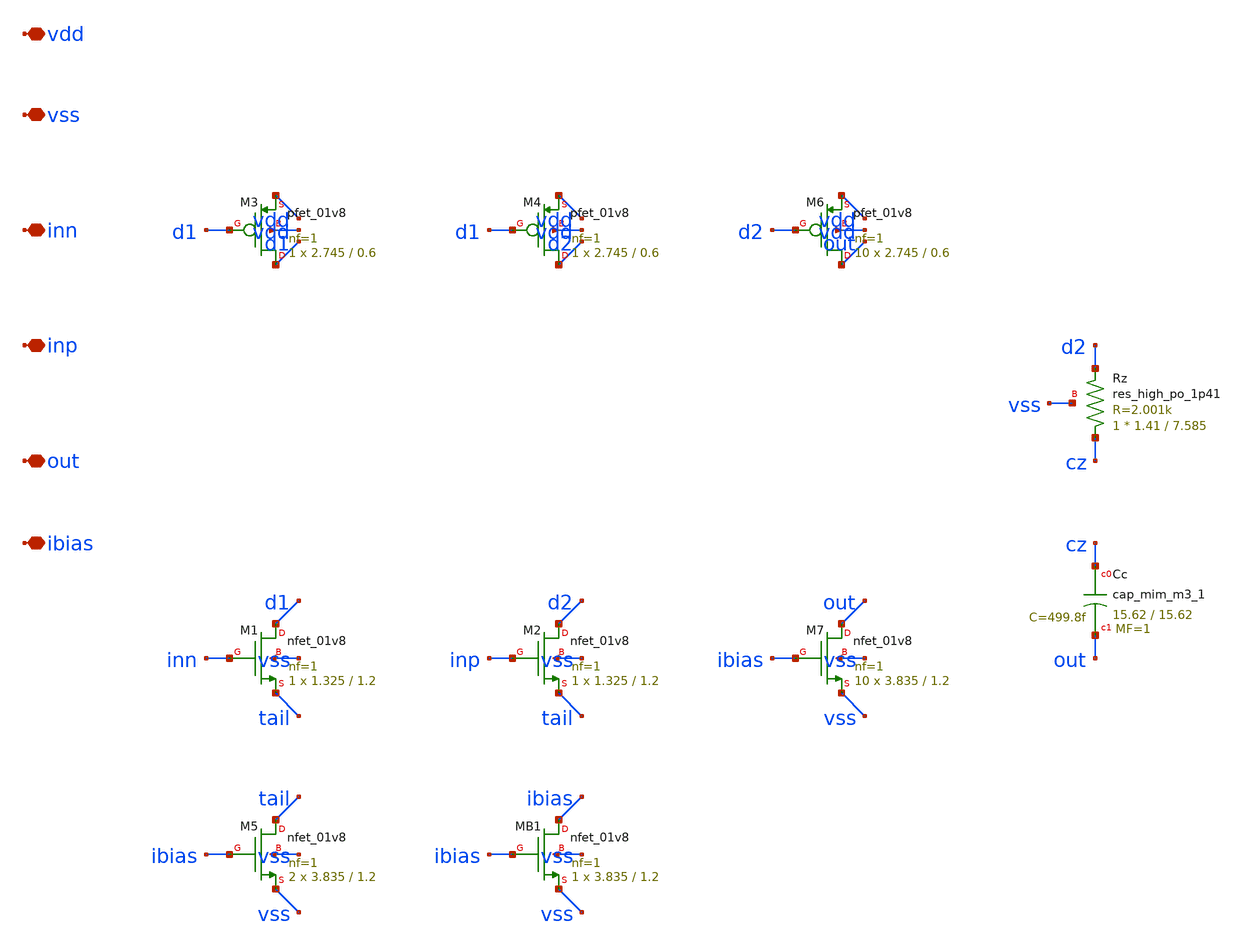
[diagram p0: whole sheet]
** sch_path: design/opamp_core.sch
**.subckt opamp_core vdd vss inn inp out ibias
*.iopin vdd
*.iopin vss
*.iopin inn
*.iopin inp
*.iopin out
*.iopin ibias
XM3 d1 d1 vdd vdd sky130_fd_pr__pfet_01v8 L=0.6 W=2.745 nf=1 ad='int((nf+1)/2) * W/nf * 0.29' as='int((nf+2)/2) * W/nf * 0.29'
+ pd='2*int((nf+1)/2) * (W/nf + 0.29)' ps='2*int((nf+2)/2) * (W/nf + 0.29)' nrd='0.29 / W' nrs='0.29 / W'
+ sa=0 sb=0 sd=0 mult=1 m=1
XM4 d2 d1 vdd vdd sky130_fd_pr__pfet_01v8 L=0.6 W=2.745 nf=1 ad='int((nf+1)/2) * W/nf * 0.29' as='int((nf+2)/2) * W/nf * 0.29'
+ pd='2*int((nf+1)/2) * (W/nf + 0.29)' ps='2*int((nf+2)/2) * (W/nf + 0.29)' nrd='0.29 / W' nrs='0.29 / W'
+ sa=0 sb=0 sd=0 mult=1 m=1
XM1 d1 inn tail vss sky130_fd_pr__nfet_01v8 L=1.2 W=1.325 nf=1 ad='int((1 + 1)/2) * 1.325 / 1 * 0.29'
+ as='int((1 + 2)/2) * 1.325 / 1 * 0.29' pd='2*int((1 + 1)/2) * (1.325 / 1 + 0.29)' ps='2*int((1 + 2)/2) * (1.325 / 1 + 0.29)'
+ nrd='0.29 / 1.325 ' nrs='0.29 / 1.325 ' sa=0 sb=0 sd=0 mult=1 m=1
XM2 d2 inp tail vss sky130_fd_pr__nfet_01v8 L=1.2 W=1.325 nf=1 ad='int((1 + 1)/2) * 1.325 / 1 * 0.29'
+ as='int((1 + 2)/2) * 1.325 / 1 * 0.29' pd='2*int((1 + 1)/2) * (1.325 / 1 + 0.29)' ps='2*int((1 + 2)/2) * (1.325 / 1 + 0.29)'
+ nrd='0.29 / 1.325 ' nrs='0.29 / 1.325 ' sa=0 sb=0 sd=0 mult=1 m=1
XM5 tail ibias vss vss sky130_fd_pr__nfet_01v8 L=1.2 W=3.835 nf=1 ad='int((1 + 1)/2) * 3.835 / 1 * 0.29'
+ as='int((1 + 2)/2) * 3.835 / 1 * 0.29' pd='2*int((1 + 1)/2) * (3.835 / 1 + 0.29)' ps='2*int((1 + 2)/2) * (3.835 / 1 + 0.29)'
+ nrd='0.29 / 3.835 ' nrs='0.29 / 3.835 ' sa=0 sb=0 sd=0 mult=2 m=2
XMB1 ibias ibias vss vss sky130_fd_pr__nfet_01v8 L=1.2 W=3.835 nf=1 ad='int((1 + 1)/2) * 3.835 / 1 * 0.29'
+ as='int((1 + 2)/2) * 3.835 / 1 * 0.29' pd='2*int((1 + 1)/2) * (3.835 / 1 + 0.29)' ps='2*int((1 + 2)/2) * (3.835 / 1 + 0.29)'
+ nrd='0.29 / 3.835 ' nrs='0.29 / 3.835 ' sa=0 sb=0 sd=0 mult=1 m=1
XM6 out d2 vdd vdd sky130_fd_pr__pfet_01v8 L=0.6 W=2.745 nf=1 ad='int((nf+1)/2) * W/nf * 0.29' as='int((nf+2)/2) * W/nf * 0.29'
+ pd='2*int((nf+1)/2) * (W/nf + 0.29)' ps='2*int((nf+2)/2) * (W/nf + 0.29)' nrd='0.29 / W' nrs='0.29 / W'
+ sa=0 sb=0 sd=0 mult=10 m=10
XM7 out ibias vss vss sky130_fd_pr__nfet_01v8 L=1.2 W=3.835 nf=1 ad='int((1 + 1)/2) * 3.835 / 1 * 0.29'
+ as='int((1 + 2)/2) * 3.835 / 1 * 0.29' pd='2*int((1 + 1)/2) * (3.835 / 1 + 0.29)' ps='2*int((1 + 2)/2) * (3.835 / 1 + 0.29)'
+ nrd='0.29 / 3.835 ' nrs='0.29 / 3.835 ' sa=0 sb=0 sd=0 mult=10 m=10
XRz cz d2 vss sky130_fd_pr__res_high_po_1p41 L=7.585 mult=1 m=1
XCc cz out sky130_fd_pr__cap_mim_m3_1 W=15.62 L=15.62 MF=1 m=1
**.ends
.end
